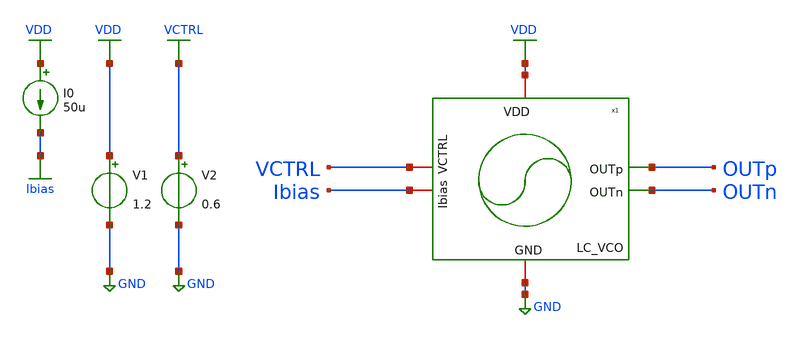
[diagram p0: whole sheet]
** sch_path: schematic/blocks/lc-vco/LC_VCO_tb.sch
**.subckt LC_VCO_tb
V1 VDD GND 1.2
V2 VCTRL GND 0.6
I0 VDD Ibias 50u
x2 VDD OUTp OUTn Ibias VCTRL GND LC_VCO
**** begin user architecture code



.include ./IHP_4nH_Inductor.spice
.param temp = 27

.control

* Initial condition
.ic v(OUTp)=0.6

* Simulation accuracy
.options reltol=1e-4 abstol=1e-9 maxstep=5p method=gear

* Save required signals
save time v(OUTp) v(CTRL)

* Long transient for ~10 kHz FFT resolution
tran 5p 100u UIC

* Save raw waveform
write LC_VCO_tb.raw

* Plot steady-state waveform
plot v(OUTp) xlimit 80u 100u

* FFT analysis
linearize v(OUTp)
fft v(OUTp)

let vmag = db(mag(v(OUTp)))

* Plot FFT spectrum
plot vmag vs frequency xlimit 0 10G

* Save FFT data
wrdata fft_output.txt frequency vmag

* Save waveform for external processing
wrdata vco_waveform.txt time v(OUTp)

.endc



 .lib cornerMOSlv.lib mos_tt
.lib cornerRES.lib res_typ
.lib $::SG13G2_MODELS/cornerCAP.lib cap_typ_stat

**** end user architecture code
**.ends

* expanding   symbol:  LC_VCO.sym # of pins=6
** sym_path: LC_VCO.sym
** sch_path: LC_VCO.sch
.subckt LC_VCO VDD OUTp OUTn Ibias VCTRL GND
*.iopin VDD
*.opin OUTp
*.opin OUTn
*.iopin GND
*.iopin VCTRL
*.iopin Ibias
XM6 net1 Ibias GND GND sg13_lv_nmos w=1u l=0.15u ng=1 m=60 mm_ok=1
XM5 Ibias Ibias GND GND sg13_lv_nmos w=1u l=0.15u ng=1 m=1 mm_ok=1
XM4 OUTp OUTn VDD VDD sg13_lv_pmos w=8.5u l=0.5u ng=1 m=13 mm_ok=1
X5M3 OUTn OUTp VDD VDD sg13_lv_pmos w=8.5u l=0.5u ng=1 m=13 mm_ok=1
XM2 OUTp OUTn net1 GND sg13_lv_nmos w=2u l=0.5u ng=1 m=12 mm_ok=1
XM1 OUTn OUTp net1 GND sg13_lv_nmos w=2u l=0.5u ng=1 m=12 mm_ok=1
XC3 OUTp OUTn cap_cmim w=4.0e-6 l=4.0e-6 m=13.6 mm_ok=1
XMv2 OUTp VCTRL OUTp VDD sg13_lv_pmos w=4u l=4u ng=1 m=22 mm_ok=1
XMv1 OUTn VCTRL OUTn VDD sg13_lv_pmos w=4u l=4u ng=1 m=22 mm_ok=1
XR1 OUTp OUTn sub! rhigh w=1e-6 l=1e-6 m=1.23 b=0 mm_ok=1
x1 OUTn OUTp ihp_4nh_inductor
.ends

.GLOBAL GND
.GLOBAL VDD
.GLOBAL VCTRL
.GLOBAL Ibias
.end
